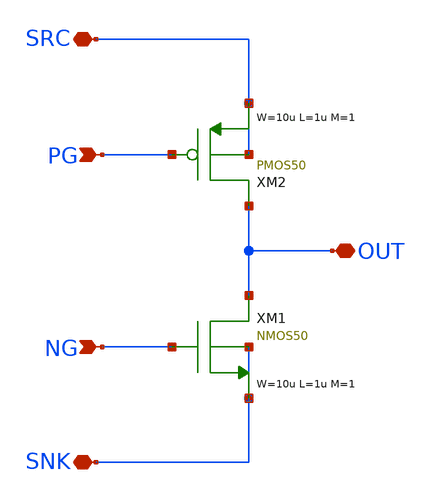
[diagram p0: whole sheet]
** sch_path: xschem/designs/CP_PowerFETs.sch
**.subckt CP_PowerFETs NG PG SRC SNK OUT
*.ipin NG
*.ipin PG
*.iopin SRC
*.iopin SNK
*.iopin OUT
XM1 OUT NG SNK SNK NMOS50 W=10u L=1u M=1 MM_SIGMA=0
XM2 OUT PG SRC SRC PMOS50 W=10u L=1u M=1 MM_SIGMA=0
**.ends
.end
